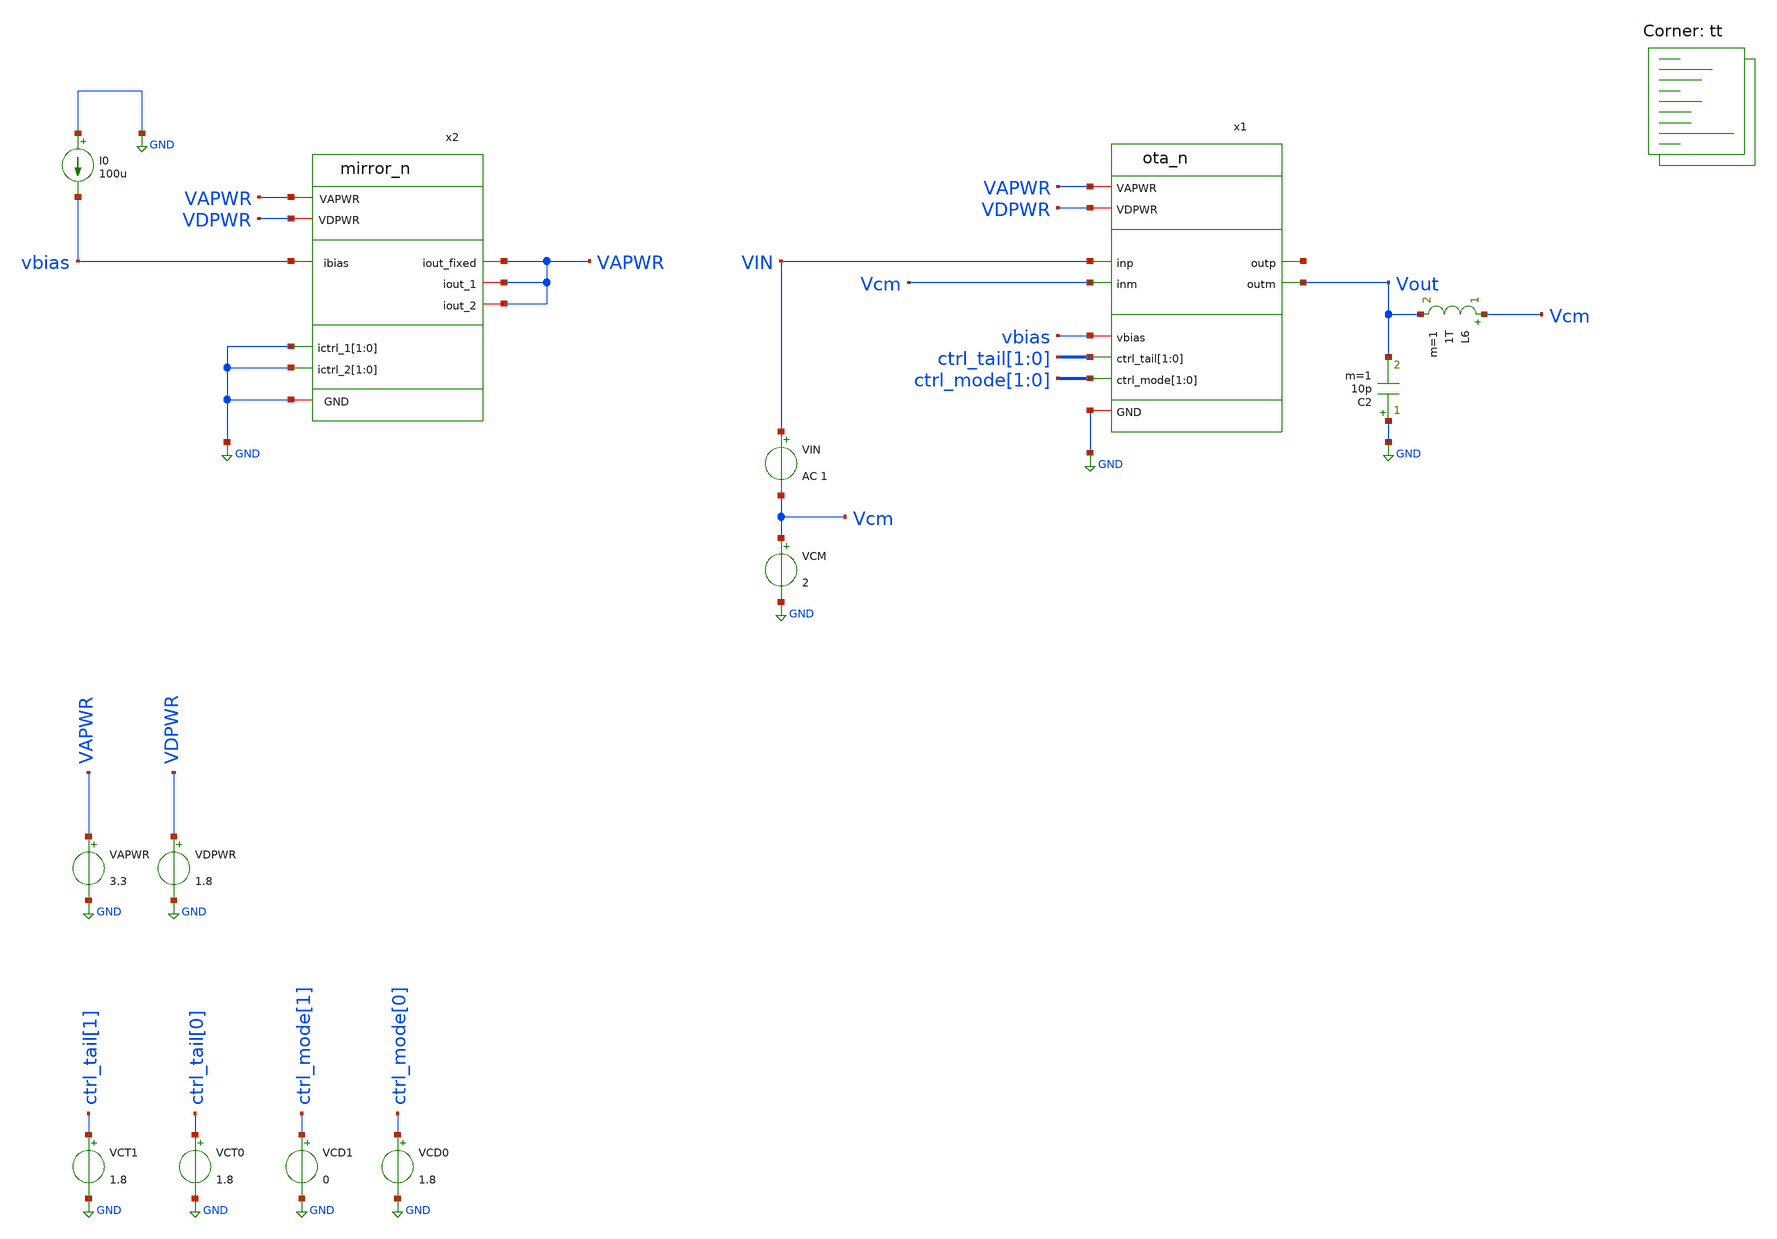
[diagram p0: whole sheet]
** sch_path: xschem/tb_ota_n_loopgain.sch
**.subckt tb_ota_n_loopgain
VAPWR VAPWR GND 3.3
VDPWR VDPWR GND 1.8
x2 VAPWR VDPWR vbias VAPWR VAPWR VAPWR GND GND GND GND GND mirror_n
I0 GND vbias 100u
VCM Vcm GND 2
VCT1 ctrl_tail[1] GND 1.8
VCT0 ctrl_tail[0] GND 1.8
VCD1 ctrl_mode[1] GND 0
VIN VIN Vcm AC 1
L6 Vcm Vout 1T m=1
C2 GND Vout 10p m=1
x1 VAPWR VDPWR VIN net1 Vcm ctrl_tail[1] ctrl_tail[0] ctrl_mode[1] ctrl_mode[0] vbias GND Vout ota_n
VCD0 ctrl_mode[0] GND 1.8
**** begin user architecture code
.lib $::SKYWATER_MODELS/sky130.lib.spice tt


*****************************************
* OTA Loop Stability Test
*****************************************
* this test steps the digital control value across full range
* and plots the current as a function of output voltage
*****************************************
.control
   save all
   set temp = 27
   set wr_singlescale
   set wr_vecnames
   alter VCM 1.5
   alter VCT1 0
   alter VCT0 0
   alter VCD 0
   repeat 2
      repeat 2
         ac dec 51 10k 1G
         alter VCT0 1.8
      end
      alter VCT1 1.8
      alter VCT0 0
   end
   plot vdb(ac1.v(Vout)) vdb(ac2.v(Vout)) vdb(ac3.v(Vout)) vdb(ac4.v(Vout))
   plot cph(ac1.v(Vout))/PI*180-180 cph(ac2.v(Vout))/PI*180-180 cph(ac3.v(Vout))/PI*180-180
+ cph(ac4.v(Vout))/PI*180-180
.endc


**** end user architecture code
**.ends
.GLOBAL GND
.end
